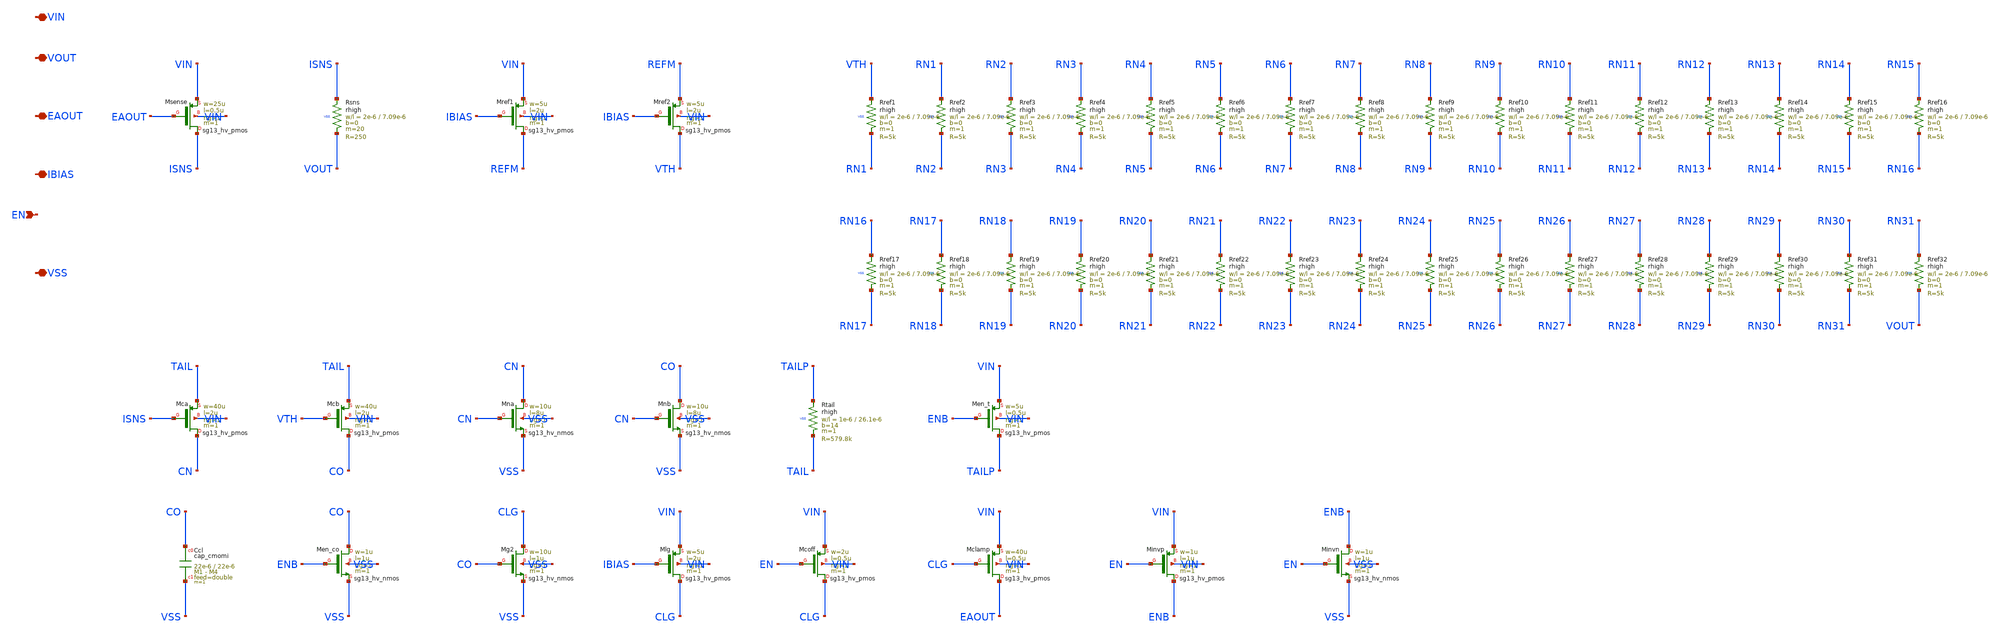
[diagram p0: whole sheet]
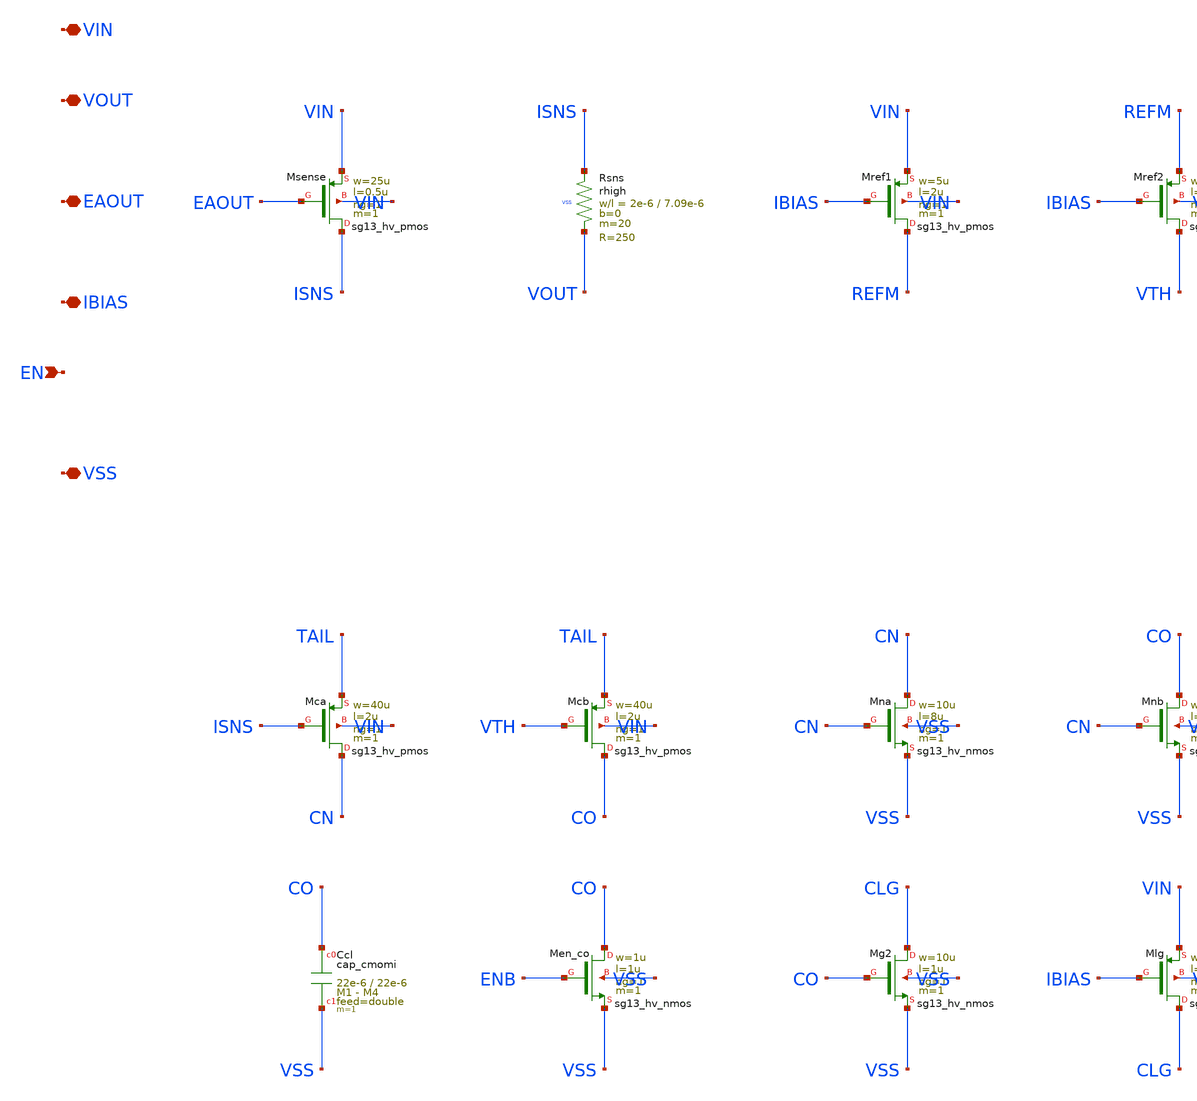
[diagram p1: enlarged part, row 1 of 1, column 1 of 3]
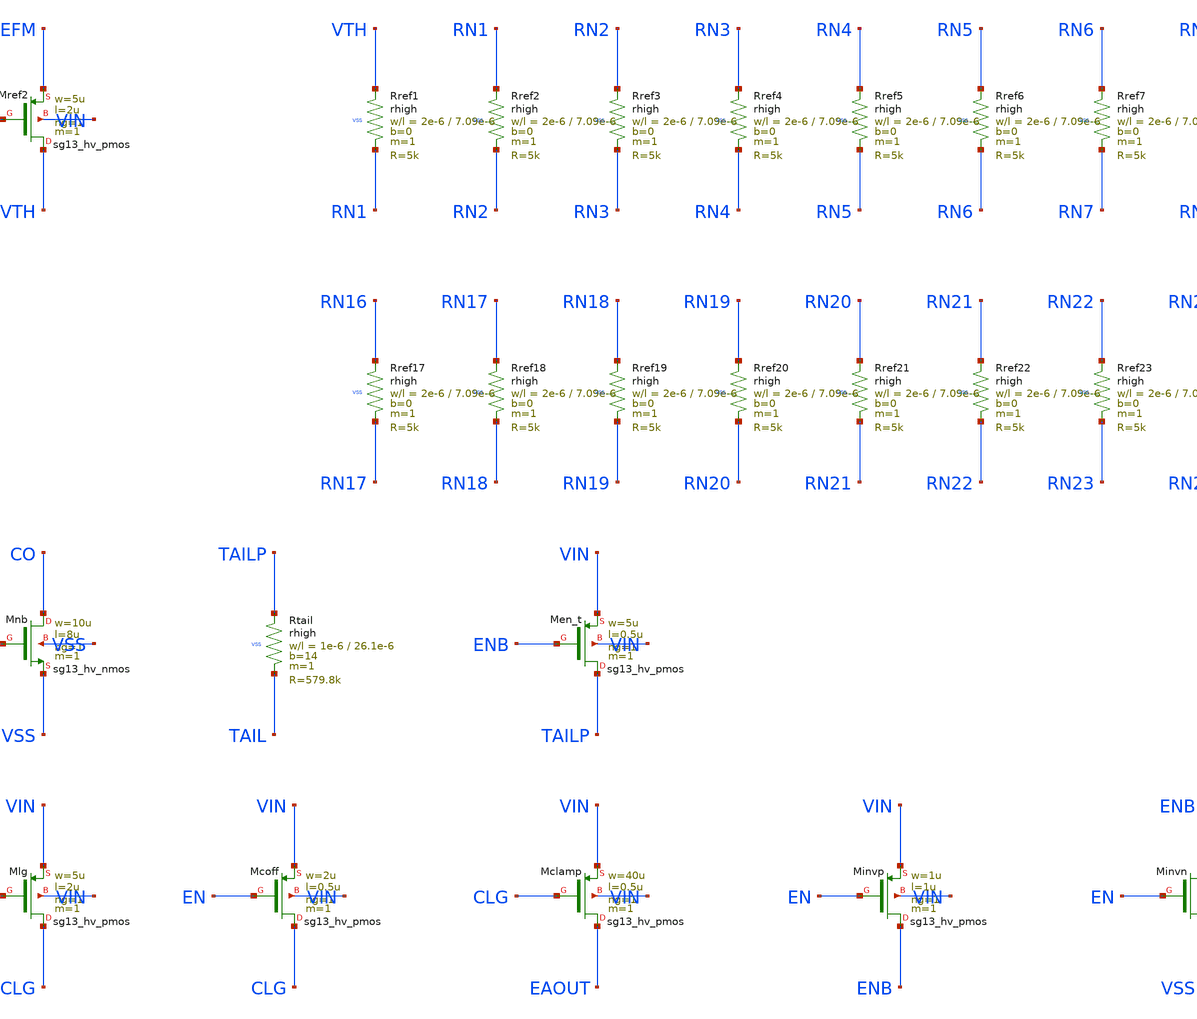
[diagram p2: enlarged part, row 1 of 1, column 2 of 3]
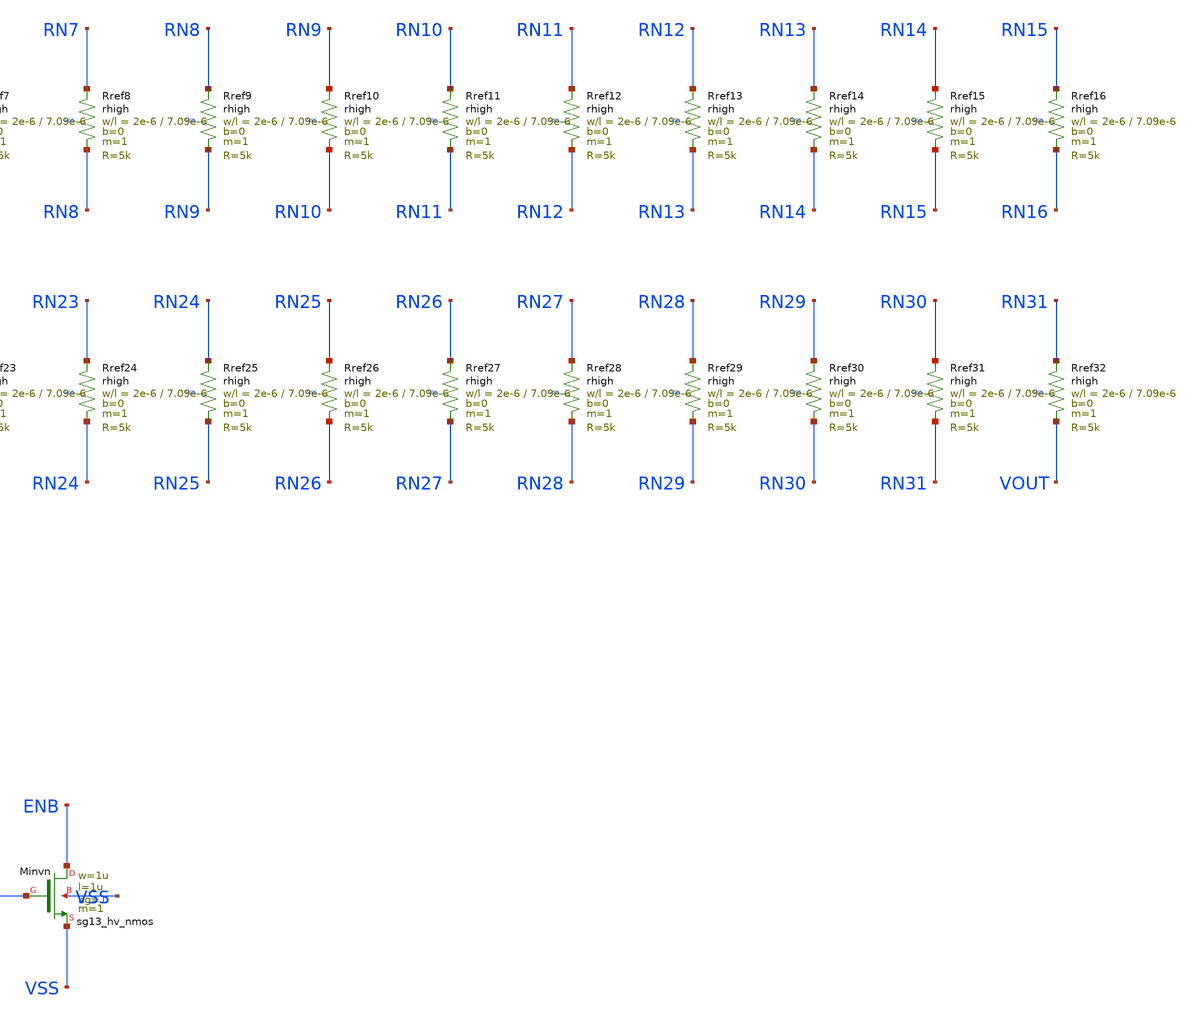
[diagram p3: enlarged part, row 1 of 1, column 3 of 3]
** sch_path: design/sg13cmos5l/ldo_ilimit_cmos5l.sch
**.subckt ldo_ilimit_cmos5l VIN VOUT EAOUT IBIAS EN VSS
*.iopin VIN
*.iopin VOUT
*.iopin EAOUT
*.iopin IBIAS
*.ipin EN
*.iopin VSS
XMsense ISNS EAOUT VIN VIN sg13_hv_pmos w=25u l=0.5u ng=1 m=1 mm_ok=1
XRsns ISNS VOUT VSS rhigh w=2e-6 l=7.09e-6 m=20 b=0 mm_ok=1
XMref1 REFM IBIAS VIN VIN sg13_hv_pmos w=5u l=2u ng=1 m=1 mm_ok=1
XMref2 VTH IBIAS REFM VIN sg13_hv_pmos w=5u l=2u ng=1 m=1 mm_ok=1
XRref1 VTH RN1 VSS rhigh w=2e-6 l=7.09e-6 m=1 b=0 mm_ok=1
XRref2 RN1 RN2 VSS rhigh w=2e-6 l=7.09e-6 m=1 b=0 mm_ok=1
XRref3 RN2 RN3 VSS rhigh w=2e-6 l=7.09e-6 m=1 b=0 mm_ok=1
XRref4 RN3 RN4 VSS rhigh w=2e-6 l=7.09e-6 m=1 b=0 mm_ok=1
XRref5 RN4 RN5 VSS rhigh w=2e-6 l=7.09e-6 m=1 b=0 mm_ok=1
XRref6 RN5 RN6 VSS rhigh w=2e-6 l=7.09e-6 m=1 b=0 mm_ok=1
XRref7 RN6 RN7 VSS rhigh w=2e-6 l=7.09e-6 m=1 b=0 mm_ok=1
XRref8 RN7 RN8 VSS rhigh w=2e-6 l=7.09e-6 m=1 b=0 mm_ok=1
XRref9 RN8 RN9 VSS rhigh w=2e-6 l=7.09e-6 m=1 b=0 mm_ok=1
XRref10 RN9 RN10 VSS rhigh w=2e-6 l=7.09e-6 m=1 b=0 mm_ok=1
XRref11 RN10 RN11 VSS rhigh w=2e-6 l=7.09e-6 m=1 b=0 mm_ok=1
XRref12 RN11 RN12 VSS rhigh w=2e-6 l=7.09e-6 m=1 b=0 mm_ok=1
XRref13 RN12 RN13 VSS rhigh w=2e-6 l=7.09e-6 m=1 b=0 mm_ok=1
XRref14 RN13 RN14 VSS rhigh w=2e-6 l=7.09e-6 m=1 b=0 mm_ok=1
XRref15 RN14 RN15 VSS rhigh w=2e-6 l=7.09e-6 m=1 b=0 mm_ok=1
XRref16 RN15 RN16 VSS rhigh w=2e-6 l=7.09e-6 m=1 b=0 mm_ok=1
XRref17 RN16 RN17 VSS rhigh w=2e-6 l=7.09e-6 m=1 b=0 mm_ok=1
XRref18 RN17 RN18 VSS rhigh w=2e-6 l=7.09e-6 m=1 b=0 mm_ok=1
XRref19 RN18 RN19 VSS rhigh w=2e-6 l=7.09e-6 m=1 b=0 mm_ok=1
XRref20 RN19 RN20 VSS rhigh w=2e-6 l=7.09e-6 m=1 b=0 mm_ok=1
XRref21 RN20 RN21 VSS rhigh w=2e-6 l=7.09e-6 m=1 b=0 mm_ok=1
XRref22 RN21 RN22 VSS rhigh w=2e-6 l=7.09e-6 m=1 b=0 mm_ok=1
XRref23 RN22 RN23 VSS rhigh w=2e-6 l=7.09e-6 m=1 b=0 mm_ok=1
XRref24 RN23 RN24 VSS rhigh w=2e-6 l=7.09e-6 m=1 b=0 mm_ok=1
XRref25 RN24 RN25 VSS rhigh w=2e-6 l=7.09e-6 m=1 b=0 mm_ok=1
XRref26 RN25 RN26 VSS rhigh w=2e-6 l=7.09e-6 m=1 b=0 mm_ok=1
XRref27 RN26 RN27 VSS rhigh w=2e-6 l=7.09e-6 m=1 b=0 mm_ok=1
XRref28 RN27 RN28 VSS rhigh w=2e-6 l=7.09e-6 m=1 b=0 mm_ok=1
XRref29 RN28 RN29 VSS rhigh w=2e-6 l=7.09e-6 m=1 b=0 mm_ok=1
XRref30 RN29 RN30 VSS rhigh w=2e-6 l=7.09e-6 m=1 b=0 mm_ok=1
XRref31 RN30 RN31 VSS rhigh w=2e-6 l=7.09e-6 m=1 b=0 mm_ok=1
XRref32 RN31 VOUT VSS rhigh w=2e-6 l=7.09e-6 m=1 b=0 mm_ok=1
XMca CN ISNS TAIL VIN sg13_hv_pmos w=40u l=2u ng=1 m=1 mm_ok=1
XMcb CO VTH TAIL VIN sg13_hv_pmos w=40u l=2u ng=1 m=1 mm_ok=1
XMna CN CN VSS VSS sg13_hv_nmos w=10u l=8u ng=1 m=1 mm_ok=1
XMnb CO CN VSS VSS sg13_hv_nmos w=10u l=8u ng=1 m=1 mm_ok=1
XRtail TAILP TAIL VSS rhigh w=1e-6 l=26.1e-6 m=1 b=14 mm_ok=1
XMen_t TAILP ENB VIN VIN sg13_hv_pmos w=5u l=0.5u ng=1 m=1 mm_ok=1
XCcl CO VSS cap_cmomi w=22e-6 l=22e-6 mmin=1 mmax=4 feed=double subblock=0 m=1 mm_ok=1
XMen_co CO ENB VSS VSS sg13_hv_nmos w=1u l=1u ng=1 m=1 mm_ok=1
XMg2 CLG CO VSS VSS sg13_hv_nmos w=10u l=1u ng=1 m=1 mm_ok=1
XMlg CLG IBIAS VIN VIN sg13_hv_pmos w=5u l=2u ng=1 m=1 mm_ok=1
XMcoff CLG EN VIN VIN sg13_hv_pmos w=2u l=0.5u ng=1 m=1 mm_ok=1
XMclamp EAOUT CLG VIN VIN sg13_hv_pmos w=40u l=0.5u ng=1 m=1 mm_ok=1
XMinvp ENB EN VIN VIN sg13_hv_pmos w=1u l=1u ng=1 m=1 mm_ok=1
XMinvn ENB EN VSS VSS sg13_hv_nmos w=1u l=1u ng=1 m=1 mm_ok=1
**.ends
.end
